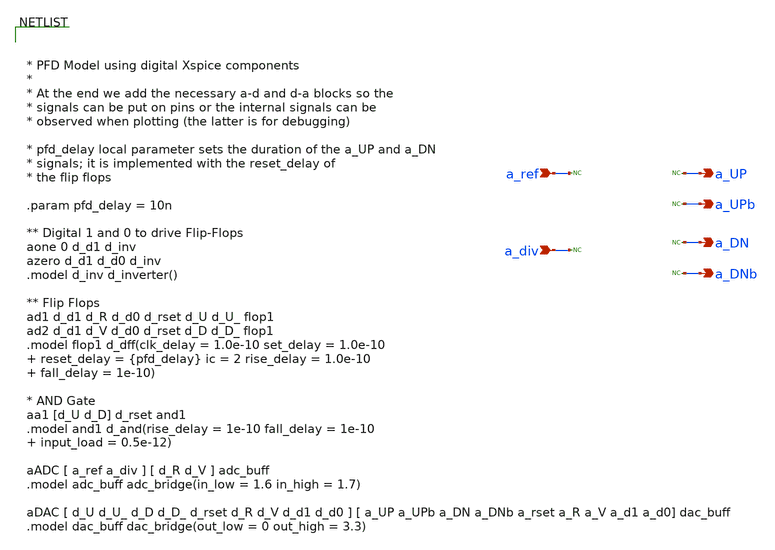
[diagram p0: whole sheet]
** sch_path: designs/libs/model_pll/pfd_model.sch
**.subckt pfd_model a_ref a_div a_UP a_UPb a_DN a_DNb
*.ipin a_ref
*.ipin a_div
*.opin a_UP
*.opin a_UPb
*.opin a_DN
*.opin a_DNb
* noconn a_ref
* noconn a_div
* noconn a_UP
* noconn a_UPb
* noconn a_DN
* noconn a_DNb
**** begin user architecture code



* PFD Model using digital Xspice components
*
* At the end we add the necessary a-d and d-a blocks so the
* signals can be put on pins or the internal signals can be
* observed when plotting (the latter is for debugging)

* pfd_delay local parameter sets the duration of the a_UP and a_DN
* signals; it is implemented with the reset_delay of
* the flip flops

.param pfd_delay = 10n

** Digital 1 and 0 to drive Flip-Flops
aone 0 d_d1 d_inv
azero d_d1 d_d0 d_inv
.model d_inv d_inverter()

** Flip Flops
ad1 d_d1 d_R d_d0 d_rset d_U d_U_ flop1
ad2 d_d1 d_V d_d0 d_rset d_D d_D_ flop1
.model flop1 d_dff(clk_delay = 1.0e-10 set_delay = 1.0e-10  reset_delay = {pfd_delay} ic = 2 rise_delay
+ = 1.0e-10  fall_delay = 1e-10)

* AND Gate
aa1 [d_U d_D] d_rset and1
.model and1 d_and(rise_delay = 1e-10 fall_delay = 1e-10  input_load = 0.5e-12)

aADC [ a_ref a_div ] [ d_R d_V ] adc_buff
.model adc_buff adc_bridge(in_low = 1.6 in_high = 1.7)

aDAC [ d_U d_U_ d_D d_D_ d_rset d_R d_V d_d1 d_d0 ] [ a_UP a_UPb a_DN a_DNb a_rset a_R a_V a_d1
+ a_d0] dac_buff
.model dac_buff dac_bridge(out_low = 0 out_high = 3.3)



**** end user architecture code
**.ends
.end
